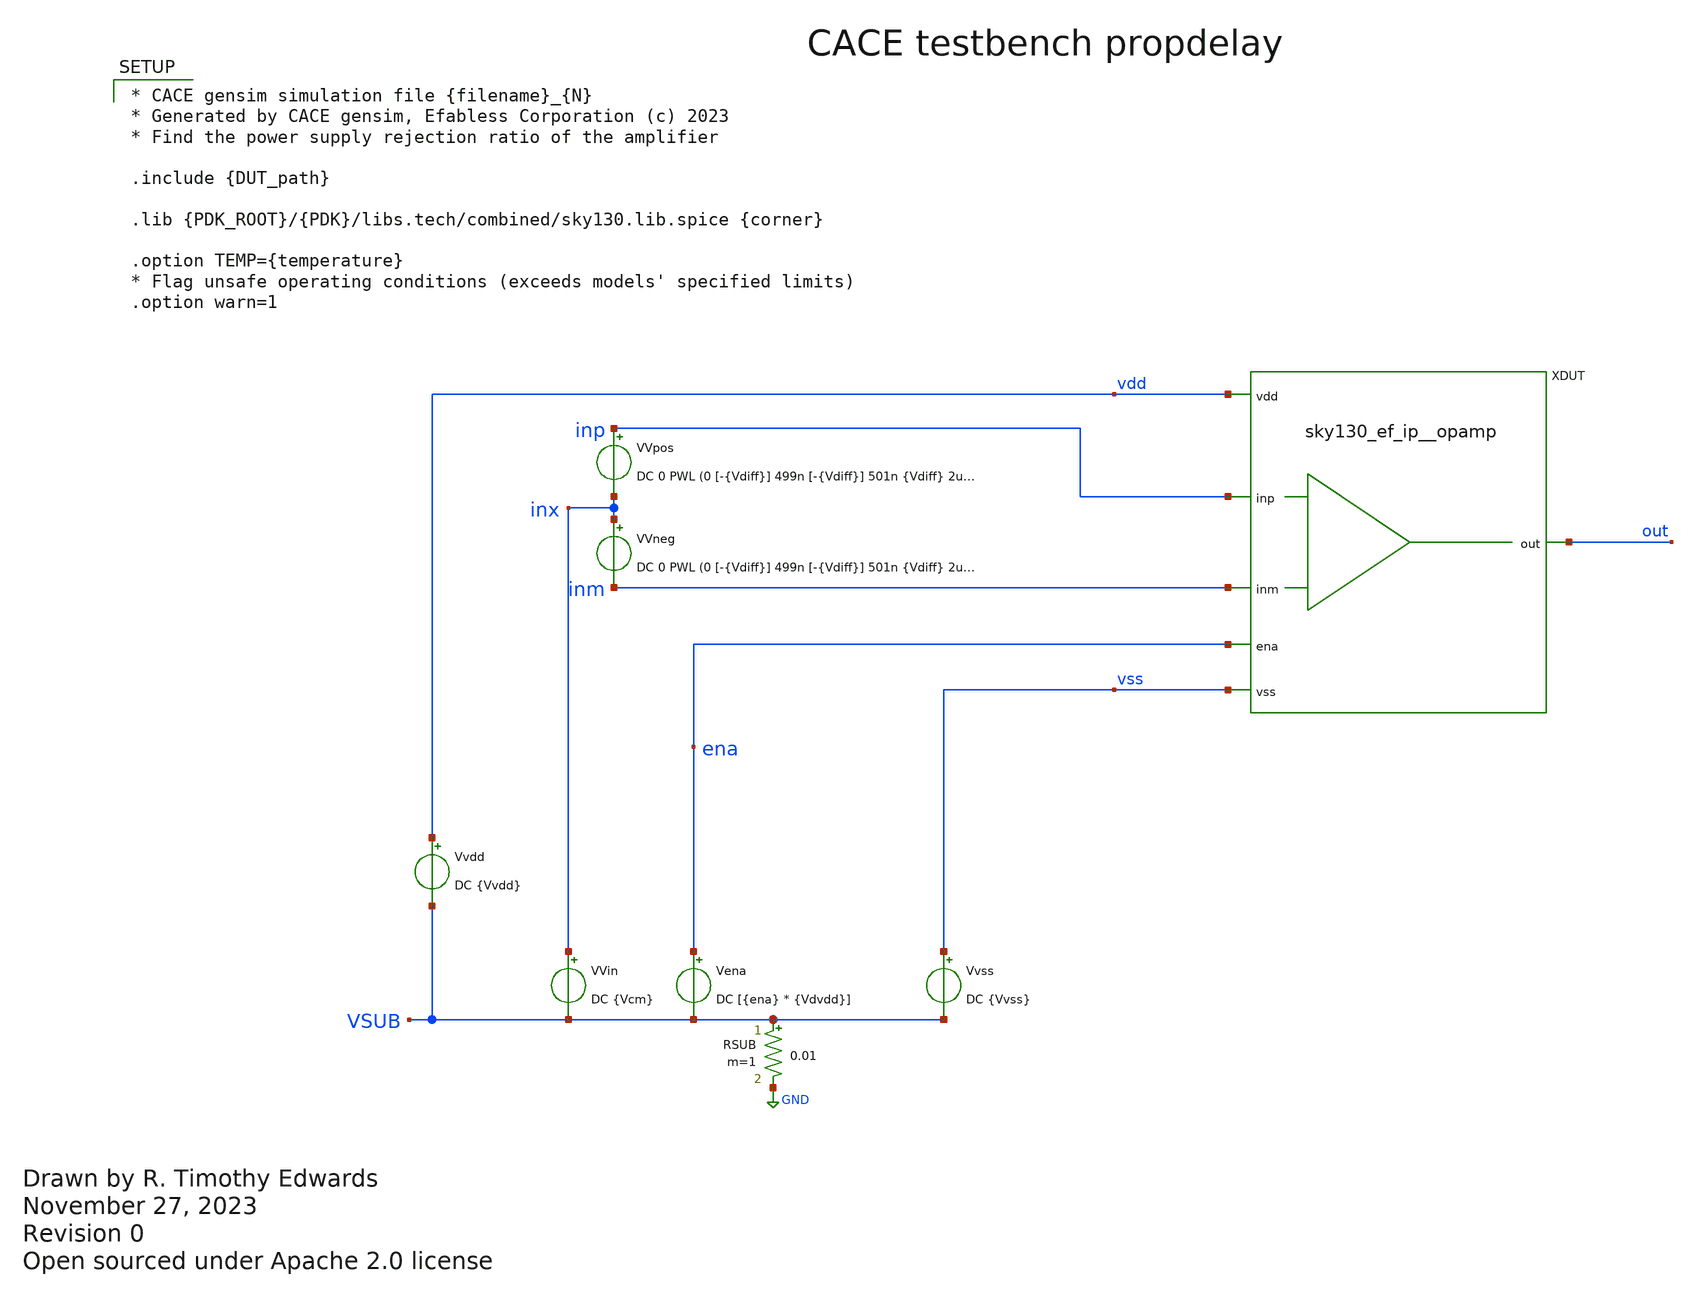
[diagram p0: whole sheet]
** sch_path: cace/templates/propdelay.sch
* Open sourced under Apache 2.0 license
**.subckt propdelay
VVin inx VSUB DC {Vcm}
Vena ena VSUB DC [{ena} * {Vdvdd}]
Vvss vss VSUB DC {Vvss}
Vvdd vdd VSUB DC {Vvdd}
RSUB VSUB GND 0.01 m=1
XDUT vdd out ena vss inp inm sky130_ef_ip__opamp
VVpos inp inx DC 0 PWL (0 [-{Vdiff}] 499n [-{Vdiff}] 501n {Vdiff} 2u {Vdiff}
VVneg inx inm DC 0 PWL (0 [-{Vdiff}] 499n [-{Vdiff}] 501n {Vdiff} 2u {Vdiff}
**** begin user architecture code

.control
** Propagation delay.  Input differential Vdiff is set to the overdrive
** voltage.  Set this to the negative of its value, then switch to the
** positive.  Measure the time for the output to change state (cross
** Vdd / 2).
tran 1e-9 2e-6
meas tran trise WHEN V(out) = [{Vvdd} / 2] CROSS=1
let tpd = $&trise - 500e-9

echo $&tpd > {simpath}/{filename}_{N}.data
quit
.endc



* CACE gensim simulation file {filename}_{N}
* Generated by CACE gensim, Efabless Corporation (c) 2023
* Find the power supply rejection ratio of the amplifier

.include {DUT_path}

.lib {PDK_ROOT}/{PDK}/libs.tech/combined/sky130.lib.spice {corner}

.option TEMP={temperature}
* Flag unsafe operating conditions (exceeds models' specified limits)
.option warn=1


**** end user architecture code
**.ends

* expanding   symbol:  sky130_ef_ip__opamp.sym # of pins=6
** sym_path: xschem/sky130_ef_ip__opamp.sym
** sch_path: xschem/sky130_ef_ip__opamp.sch
.subckt sky130_ef_ip__opamp vdd out ena vss inp inm
*.ipin inp
*.ipin vdd
*.ipin vss
*.opin out
*.ipin ena
*.ipin inm
XM4 pdrv1 net1 vdd vdd sky130_fd_pr__pfet_g5v0d10v5 L=0.5 W=2 nf=2 ad='int((nf+1)/2) * W/nf * 0.29' as='int((nf+2)/2)
+ * W/nf * 0.29' pd='2*int((nf+1)/2) * (W/nf + 0.29)' ps='2*int((nf+2)/2) * (W/nf + 0.29)' nrd='0.29 /
+ W' nrs='0.29 / W' sa=0 sb=0 sd=0 mult=1 m=1
XM5 vdd net1 net1 vdd sky130_fd_pr__pfet_g5v0d10v5 L=0.5 W=2 nf=2 ad='int((nf+1)/2) * W/nf * 0.29' as='int((nf+2)/2)
+ * W/nf * 0.29' pd='2*int((nf+1)/2) * (W/nf + 0.29)' ps='2*int((nf+2)/2) * (W/nf + 0.29)' nrd='0.29 /
+ W' nrs='0.29 / W' sa=0 sb=0 sd=0 mult=1 m=1
XM9 vcomn1 nbias vss vss sky130_fd_pr__nfet_g5v0d10v5 L=0.5 W=1 nf=1 ad='int((nf+1)/2) * W/nf * 0.29' as='int((nf+2)/2)
+ * W/nf * 0.29' pd='2*int((nf+1)/2) * (W/nf + 0.29)' ps='2*int((nf+2)/2) * (W/nf + 0.29)' nrd='0.29 /
+ W' nrs='0.29 / W' sa=0 sb=0 sd=0 mult=1 m=1
XM10 vss nbias nbias vss sky130_fd_pr__nfet_g5v0d10v5 L=0.5 W=4 nf=4 ad='int((nf+1)/2) * W/nf * 0.29' as='int((nf+2)/2)
+ * W/nf * 0.29' pd='2*int((nf+1)/2) * (W/nf + 0.29)' ps='2*int((nf+2)/2) * (W/nf + 0.29)' nrd='0.29 /
+ W' nrs='0.29 / W' sa=0 sb=0 sd=0 mult=1 m=1
XR1 net4 vdd vss sky130_fd_pr__res_xhigh_po_0p35 L=100 mult=1 m=1
XM20 out pdrv1 vdd vdd sky130_fd_pr__pfet_g5v0d10v5 L=0.5 W=200 nf=200 ad='int((nf+1)/2) * W/nf * 0.29' as='int((nf+2)/2)
+ * W/nf * 0.29' pd='2*int((nf+1)/2) * (W/nf + 0.29)' ps='2*int((nf+2)/2) * (W/nf + 0.29)' nrd='0.29 /
+ W' nrs='0.29 / W' sa=0 sb=0 sd=0 mult=1 m=1
XM22 out ndrv vss vss sky130_fd_pr__nfet_g5v0d10v5 L=0.5 W=120 nf=120 ad='int((nf+1)/2) * W/nf * 0.29' as='int((nf+2)/2)
+ * W/nf * 0.29' pd='2*int((nf+1)/2) * (W/nf + 0.29)' ps='2*int((nf+2)/2) * (W/nf + 0.29)' nrd='0.29 /
+ W' nrs='0.29 / W' sa=0 sb=0 sd=0 mult=1 m=1
XM24 pbias nbias vss vss sky130_fd_pr__nfet_g5v0d10v5 L=0.5 W=1 nf=1 ad='int((nf+1)/2) * W/nf * 0.29' as='int((nf+2)/2)
+ * W/nf * 0.29' pd='2*int((nf+1)/2) * (W/nf + 0.29)' ps='2*int((nf+2)/2) * (W/nf + 0.29)' nrd='0.29 /
+ W' nrs='0.29 / W' sa=0 sb=0 sd=0 mult=1 m=1
XM25 vdd pbias pbias vdd sky130_fd_pr__pfet_g5v0d10v5 L=0.5 W=1 nf=1 ad='int((nf+1)/2) * W/nf * 0.29' as='int((nf+2)/2)
+ * W/nf * 0.29' pd='2*int((nf+1)/2) * (W/nf + 0.29)' ps='2*int((nf+2)/2) * (W/nf + 0.29)' nrd='0.29 /
+ W' nrs='0.29 / W' sa=0 sb=0 sd=0 mult=1 m=1
XM26 vcomp pbias vdd vdd sky130_fd_pr__pfet_g5v0d10v5 L=0.5 W=2 nf=2 ad='int((nf+1)/2) * W/nf * 0.29' as='int((nf+2)/2)
+ * W/nf * 0.29' pd='2*int((nf+1)/2) * (W/nf + 0.29)' ps='2*int((nf+2)/2) * (W/nf + 0.29)' nrd='0.29 /
+ W' nrs='0.29 / W' sa=0 sb=0 sd=0 mult=1 m=1
XM27 net2 inm vcomp vdd sky130_fd_pr__pfet_g5v0d10v5 L=0.5 W=2 nf=2 ad='int((nf+1)/2) * W/nf * 0.29' as='int((nf+2)/2)
+ * W/nf * 0.29' pd='2*int((nf+1)/2) * (W/nf + 0.29)' ps='2*int((nf+2)/2) * (W/nf + 0.29)' nrd='0.29 /
+ W' nrs='0.29 / W' sa=0 sb=0 sd=0 mult=1 m=1
XM28 vcomp inp ndrv vdd sky130_fd_pr__pfet_g5v0d10v5 L=0.5 W=2 nf=2 ad='int((nf+1)/2) * W/nf * 0.29' as='int((nf+2)/2)
+ * W/nf * 0.29' pd='2*int((nf+1)/2) * (W/nf + 0.29)' ps='2*int((nf+2)/2) * (W/nf + 0.29)' nrd='0.29 /
+ W' nrs='0.29 / W' sa=0 sb=0 sd=0 mult=1 m=1
XM29 ndrv net2 vss vss sky130_fd_pr__nfet_g5v0d10v5 L=0.5 W=1 nf=1 ad='int((nf+1)/2) * W/nf * 0.29' as='int((nf+2)/2)
+ * W/nf * 0.29' pd='2*int((nf+1)/2) * (W/nf + 0.29)' ps='2*int((nf+2)/2) * (W/nf + 0.29)' nrd='0.29 /
+ W' nrs='0.29 / W' sa=0 sb=0 sd=0 mult=1 m=1
XM30 vss net2 net2 vss sky130_fd_pr__nfet_g5v0d10v5 L=0.5 W=1 nf=1 ad='int((nf+1)/2) * W/nf * 0.29' as='int((nf+2)/2)
+ * W/nf * 0.29' pd='2*int((nf+1)/2) * (W/nf + 0.29)' ps='2*int((nf+2)/2) * (W/nf + 0.29)' nrd='0.29 /
+ W' nrs='0.29 / W' sa=0 sb=0 sd=0 mult=1 m=1
XM1 net1 inm vcomn1 vss sky130_fd_pr__nfet_g5v0d10v5 L=0.5 W=1 nf=1 ad='int((nf+1)/2) * W/nf * 0.29' as='int((nf+2)/2)
+ * W/nf * 0.29' pd='2*int((nf+1)/2) * (W/nf + 0.29)' ps='2*int((nf+2)/2) * (W/nf + 0.29)' nrd='0.29 /
+ W' nrs='0.29 / W' sa=0 sb=0 sd=0 mult=1 m=1
XM2 vcomn1 inp pdrv1 vss sky130_fd_pr__nfet_g5v0d10v5 L=0.5 W=1 nf=1 ad='int((nf+1)/2) * W/nf * 0.29' as='int((nf+2)/2)
+ * W/nf * 0.29' pd='2*int((nf+1)/2) * (W/nf + 0.29)' ps='2*int((nf+2)/2) * (W/nf + 0.29)' nrd='0.29 /
+ W' nrs='0.29 / W' sa=0 sb=0 sd=0 mult=1 m=1
XM3 pdrv2 net3 vdd vdd sky130_fd_pr__pfet_g5v0d10v5 L=0.5 W=2 nf=2 ad='int((nf+1)/2) * W/nf * 0.29' as='int((nf+2)/2)
+ * W/nf * 0.29' pd='2*int((nf+1)/2) * (W/nf + 0.29)' ps='2*int((nf+2)/2) * (W/nf + 0.29)' nrd='0.29 /
+ W' nrs='0.29 / W' sa=0 sb=0 sd=0 mult=1 m=1
XM6 vdd net3 net3 vdd sky130_fd_pr__pfet_g5v0d10v5 L=0.5 W=2 nf=2 ad='int((nf+1)/2) * W/nf * 0.29' as='int((nf+2)/2)
+ * W/nf * 0.29' pd='2*int((nf+1)/2) * (W/nf + 0.29)' ps='2*int((nf+2)/2) * (W/nf + 0.29)' nrd='0.29 /
+ W' nrs='0.29 / W' sa=0 sb=0 sd=0 mult=1 m=1
XM7 vcomn2 nbias vss vss sky130_fd_pr__nfet_g5v0d10v5 L=0.5 W=1 nf=1 ad='int((nf+1)/2) * W/nf * 0.29' as='int((nf+2)/2)
+ * W/nf * 0.29' pd='2*int((nf+1)/2) * (W/nf + 0.29)' ps='2*int((nf+2)/2) * (W/nf + 0.29)' nrd='0.29 /
+ W' nrs='0.29 / W' sa=0 sb=0 sd=0 mult=1 m=1
XM8 net3 inm vcomn2 vss sky130_fd_pr__nfet_03v3_nvt L=0.5 W=1 nf=1 ad='int((nf+1)/2) * W/nf * 0.29' as='int((nf+2)/2)
+ * W/nf * 0.29' pd='2*int((nf+1)/2) * (W/nf + 0.29)' ps='2*int((nf+2)/2) * (W/nf + 0.29)' nrd='0.29 /
+ W' nrs='0.29 / W' sa=0 sb=0 sd=0 mult=1 m=1
XM11 vcomn2 inp pdrv2 vss sky130_fd_pr__nfet_03v3_nvt L=0.5 W=1 nf=1 ad='int((nf+1)/2) * W/nf * 0.29' as='int((nf+2)/2)
+ * W/nf * 0.29' pd='2*int((nf+1)/2) * (W/nf + 0.29)' ps='2*int((nf+2)/2) * (W/nf + 0.29)' nrd='0.29 /
+ W' nrs='0.29 / W' sa=0 sb=0 sd=0 mult=1 m=1
XM12 vdd pdrv2 out vdd sky130_fd_pr__pfet_g5v0d10v5 L=0.5 W=200 nf=200 ad='int((nf+1)/2) * W/nf * 0.29' as='int((nf+2)/2)
+ * W/nf * 0.29' pd='2*int((nf+1)/2) * (W/nf + 0.29)' ps='2*int((nf+2)/2) * (W/nf + 0.29)' nrd='0.29 /
+ W' nrs='0.29 / W' sa=0 sb=0 sd=0 mult=1 m=1
XXD1 vss inp sky130_fd_pr__diode_pw2nd_05v5 area=3.6e11 pj=4e6
XM13 net4 ena nbias vss sky130_fd_pr__nfet_g5v0d10v5 L=0.5 W=1 nf=1 ad='int((nf+1)/2) * W/nf * 0.29' as='int((nf+2)/2)
+ * W/nf * 0.29' pd='2*int((nf+1)/2) * (W/nf + 0.29)' ps='2*int((nf+2)/2) * (W/nf + 0.29)' nrd='0.29 /
+ W' nrs='0.29 / W' sa=0 sb=0 sd=0 mult=1 m=1
XXD2 vss ena sky130_fd_pr__diode_pw2nd_05v5 area=3.6e11 pj=4e6
XXD3 vss inm sky130_fd_pr__diode_pw2nd_05v5 area=3.6e11 pj=4e6
.ends

.GLOBAL GND
.end
